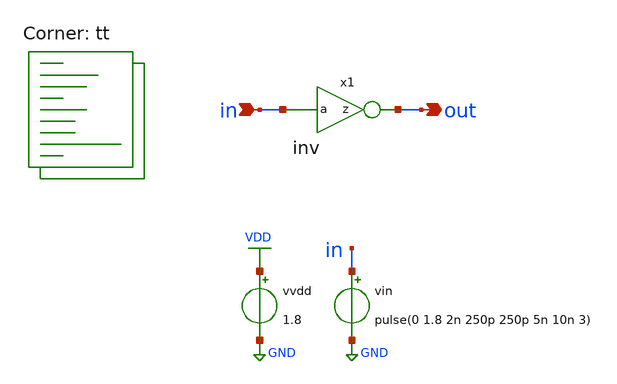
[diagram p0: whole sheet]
** sch_path: xschem/sim/tb_inv.sch
**.subckt tb_inv in out
*.ipin in
*.opin out
x1 out in inv
vvdd VDD GND 1.8
vin in GND pulse(0 1.8 2n 250p 250p 5n 10n 3)
**** begin user architecture code
.lib $::SKYWATER_MODELS/sky130.lib.spice tt


.control
* VTC analysis
DC vin 0 1.8 1m
save all
let VP = 1.8
let vo_mid = VP/2
let dvout = deriv(v(out))
meas DC VSW find v(in) when v(out)=vo_mid
meas DC VIL find v(in) WHEN dvout=-1 CROSS=1
meas DC VIH find v(in) WHEN dvout=-1 CROSS=2
meas DC VOL find v(out) WHEN dvout=-1 CROSS=2
meas DC VOH find v(out) WHEN dvout=-1 CROSS=1
echo VTC measurements
print VSW
print VIL
print VIH
print VOH
print VOL
echo
set filetype=binary
write tb_inv_vtc.raw v(out) v(in) dvout VSW VIL VIH VOH VOL

* Transient analysis
TRAN 1p 40n
save all
let VP=1.8
let per10 = Vp*0.1
let per50 = Vp*0.5
let per90 = Vp*0.9
meas TRAN t_rise  TRIG v(out) VAL=per10 rise=1  TARG v(out) VAL=per90 rise=1
meas TRAN t_fall  TRIG v(out) VAL=per90 fall=1  TARG v(out) VAL=per10 fall=1
meas TRAN t_delay  TRIG v(in) VAL=per50 rise=1 TARG v(out) VAL=per50 fall=1
echo TRAN measurements
print t_delay
print t_rise
print t_fall
echo
set filetype=binary
write tb_inv_tran.raw
.endc


**** end user architecture code
**.ends
.GLOBAL VDD
.GLOBAL GND
.end
